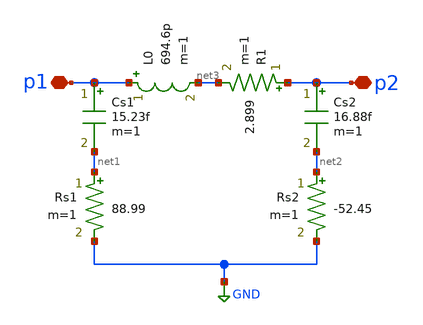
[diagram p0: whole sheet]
** sch_path: impedance-transformer/xschem/l1.sch
**.subckt l1 p2 p1
*.iopin p2
*.iopin p1
L0 p1 net3 694.6p m=1
Cs1 p1 net1 15.23f m=1
Cs2 p2 net2 16.88f m=1
Rs1 net1 GND 88.99 m=1
Rs2 net2 GND -52.45 m=1
R1 p2 net3 2.899 m=1
**.ends
.GLOBAL GND
.end
